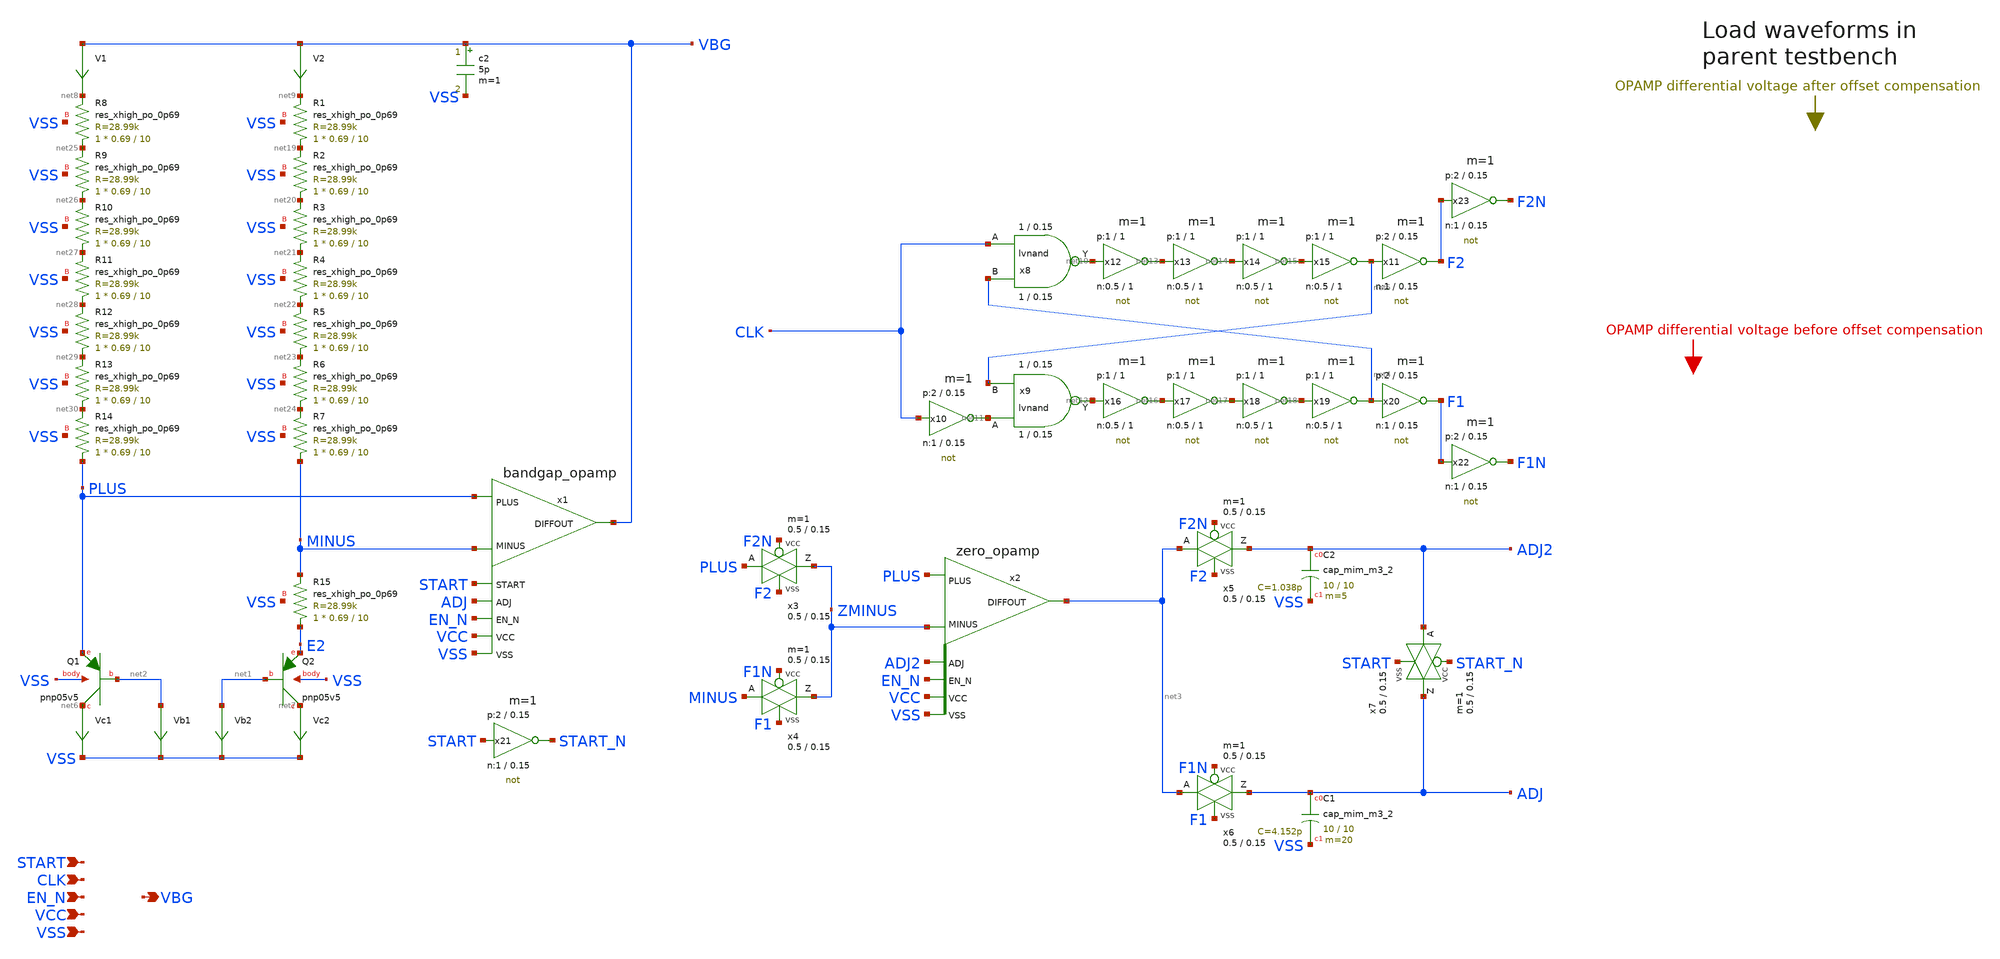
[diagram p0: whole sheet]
** sch_path: sky130_tests/bandgap.sch
* Copyright 2021 Stefan Frederik Schippers
* Licensed under the Apache License, Version 2.0 (the "License");
* you may not use this file except in compliance with the License.
* You may obtain a copy of the License at
* https://www.apache.org/licenses/LICENSE-2.0
* Unless required by applicable law or agreed to in writing, software
* distributed under the License is distributed on an "AS IS" BASIS,
* WITHOUT WARRANTIES OR CONDITIONS OF ANY KIND, either express or implied.
* See the License for the specific language governing permissions and
* limitations under the License.
**.subckt bandgap EN_N VBG VCC VSS CLK START
*.ipin EN_N
*.opin VBG
*.ipin VCC
*.ipin VSS
*.ipin CLK
*.ipin START
XQ1 net6 net2 PLUS VSS sky130_fd_pr__pnp_05v5_W0p68L0p68 m=1
XQ2 net7 net1 E2 VSS sky130_fd_pr__pnp_05v5_W0p68L0p68 m=8
Vc1 net6 VSS 0
.save i(vc1)
Vb1 net2 VSS 0
.save i(vb1)
Vb2 net1 VSS 0
.save i(vb2)
Vc2 net7 VSS 0
.save i(vc2)
x1 EN_N MINUS PLUS VBG VCC VSS ADJ START bandgap_opamp
V1 VBG net8 0
.save i(v1)
V2 VBG net9 0
.save i(v2)
x2 EN_N ZMINUS PLUS net3 VCC VSS ADJ2 zero_opamp
x3 ZMINUS PLUS F2N F2 VCC VSS passgate W_N=0.5 L_N=0.15 W_P=0.5 L_P=0.15 m=1
x4 ZMINUS MINUS F1N F1 VCC VSS passgate W_N=0.5 L_N=0.15 W_P=0.5 L_P=0.15 m=1
x5 ADJ2 net3 F2N F2 VCC VSS passgate W_N=0.5 L_N=0.15 W_P=0.5 L_P=0.15 m=1
x6 ADJ net3 F1N F1 VCC VSS passgate W_N=0.5 L_N=0.15 W_P=0.5 L_P=0.15 m=1
x8 CLK net4 net10 lvnand WidthN=1 LenN=0.15 WidthP=1 LenP=0.15 m=1
x9 net11 net5 net12 lvnand WidthN=1 LenN=0.15 WidthP=1 LenP=0.15 m=1
x10 net11 CLK VCC VSS not W_N=1 L_N=0.15 W_P=2 L_P=0.15 m=1
x11 F2 net5 VCC VSS not W_N=1 L_N=0.15 W_P=2 L_P=0.15 m=1
x12 net13 net10 VCC VSS not W_N=0.5 L_N=1 W_P=1 L_P=1 m=1
x13 net14 net13 VCC VSS not W_N=0.5 L_N=1 W_P=1 L_P=1 m=1
x14 net15 net14 VCC VSS not W_N=0.5 L_N=1 W_P=1 L_P=1 m=1
x15 net5 net15 VCC VSS not W_N=0.5 L_N=1 W_P=1 L_P=1 m=1
x16 net16 net12 VCC VSS not W_N=0.5 L_N=1 W_P=1 L_P=1 m=1
x17 net17 net16 VCC VSS not W_N=0.5 L_N=1 W_P=1 L_P=1 m=1
x18 net18 net17 VCC VSS not W_N=0.5 L_N=1 W_P=1 L_P=1 m=1
x19 net4 net18 VCC VSS not W_N=0.5 L_N=1 W_P=1 L_P=1 m=1
x20 F1 net4 VCC VSS not W_N=1 L_N=0.15 W_P=2 L_P=0.15 m=1
c2 VBG VSS 5p m=1
x7 ADJ ADJ2 START_N START VCC VSS passgate W_N=0.5 L_N=0.15 W_P=0.5 L_P=0.15 m=1
x21 START_N START VCC VSS not W_N=1 L_N=0.15 W_P=2 L_P=0.15 m=1
x22 F1N F1 VCC VSS not W_N=1 L_N=0.15 W_P=2 L_P=0.15 m=1
x23 F2N F2 VCC VSS not W_N=1 L_N=0.15 W_P=2 L_P=0.15 m=1
XC2 ADJ2 VSS sky130_fd_pr__cap_mim_m3_2 W=10 L=10 MF=5 m=5
XC1 ADJ VSS sky130_fd_pr__cap_mim_m3_2 W=10 L=10 MF=20 m=20
XR1 net19 net9 VSS sky130_fd_pr__res_xhigh_po_0p69 L=10 mult=1 m=1
XR2 net20 net19 VSS sky130_fd_pr__res_xhigh_po_0p69 L=10 mult=1 m=1
XR3 net21 net20 VSS sky130_fd_pr__res_xhigh_po_0p69 L=10 mult=1 m=1
XR4 net22 net21 VSS sky130_fd_pr__res_xhigh_po_0p69 L=10 mult=1 m=1
XR5 net23 net22 VSS sky130_fd_pr__res_xhigh_po_0p69 L=10 mult=1 m=1
XR6 net24 net23 VSS sky130_fd_pr__res_xhigh_po_0p69 L=10 mult=1 m=1
XR7 MINUS net24 VSS sky130_fd_pr__res_xhigh_po_0p69 L=10 mult=1 m=1
XR8 net25 net8 VSS sky130_fd_pr__res_xhigh_po_0p69 L=10 mult=1 m=1
XR9 net26 net25 VSS sky130_fd_pr__res_xhigh_po_0p69 L=10 mult=1 m=1
XR10 net27 net26 VSS sky130_fd_pr__res_xhigh_po_0p69 L=10 mult=1 m=1
XR11 net28 net27 VSS sky130_fd_pr__res_xhigh_po_0p69 L=10 mult=1 m=1
XR12 net29 net28 VSS sky130_fd_pr__res_xhigh_po_0p69 L=10 mult=1 m=1
XR13 net30 net29 VSS sky130_fd_pr__res_xhigh_po_0p69 L=10 mult=1 m=1
XR14 PLUS net30 VSS sky130_fd_pr__res_xhigh_po_0p69 L=10 mult=1 m=1
XR15 E2 MINUS VSS sky130_fd_pr__res_xhigh_po_0p69 L=10 mult=1 m=1
**.ends
.end
